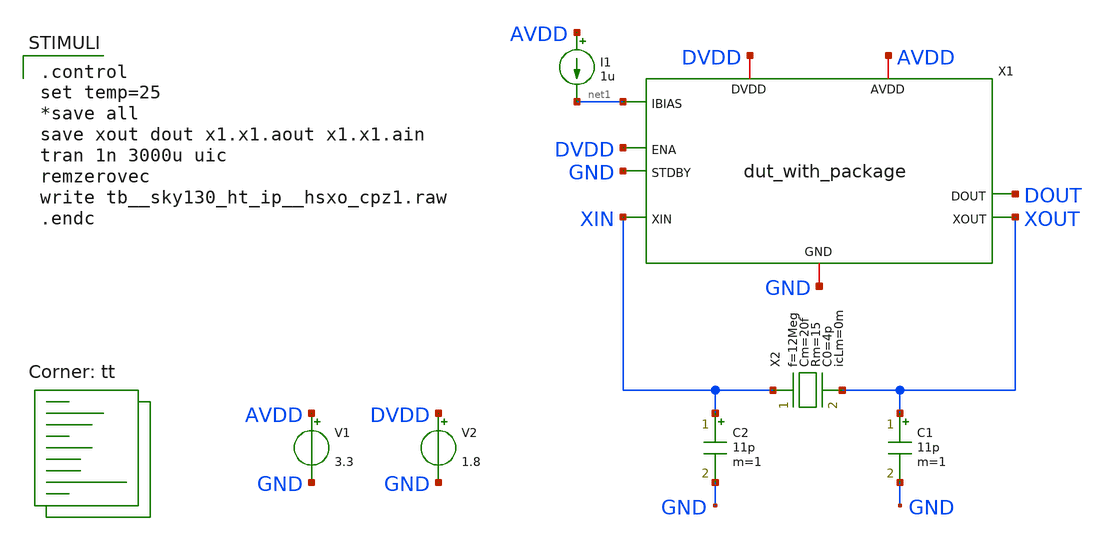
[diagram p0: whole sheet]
** sch_path: xschem/tb__sky130_ht_ip__hsxo_cpz1.sch
**.subckt tb__sky130_ht_ip__hsxo_cpz1
X1 XOUT XIN DVDD GND DOUT AVDD DVDD GND net1 dut_with_package
C1 XOUT GND 11p m=1
C2 XIN GND 11p m=1
I1 AVDD net1 1u
V1 AVDD GND 3.3
V2 DVDD GND 1.8
X2 XIN XOUT crystal_model_p_res f=12Meg Cm=20f Rm=15 C0=4p icLm=0m
**** begin user architecture code
.lib $::SKYWATER_MODELS/sky130.lib.spice tt

.control
set temp=25
*save all
save xout dout x1.x1.aout x1.x1.ain
tran 1n 3000u uic
remzerovec
write tb__sky130_ht_ip__hsxo_cpz1.raw
.endc


**** end user architecture code
**.ends

* expanding   symbol:  dut_with_package.sym # of pins=9
** sym_path: xschem/dut_with_package.sym
** sch_path: xschem/dut_with_package.sch
.subckt dut_with_package XOUT XIN ENA STDBY DOUT AVDD DVDD GND IBIAS
*.iopin DVDD
*.iopin GND
*.iopin AVDD
*.ipin ENA
*.ipin STDBY
*.ipin XIN
*.opin XOUT
*.opin DOUT
*.ipin IBIAS
X1 XOUTPAD XINPAD ENA STDBY DOUT AVDD DVDD AVSS GND IBIAS sky130_ht_ip__hsxo_cpz1
X2 XIN GND XINPAD XOUTPAD XOUT GND AVSS package_model
.ends


* expanding   symbol:  crystal_model_p_res.sym # of pins=2
** sym_path: xschem/crystal_model_p_res.sym
** sch_path: xschem/crystal_model_p_res.sch
.subckt crystal_model_p_res XIN XOUT  f=12Meg Cm=20f Rm=15 C0=4p icLm=0m
*.iopin XIN
*.iopin XOUT
X1 XIN XOUT crystal_model Lm=(1/Cm+1/C0)/(4*pi^2*f^2) Cm=Cm Rm=Rm C0=C0 icLm=icLm
**** begin user architecture code
.param pi=4*atan(1)
**** end user architecture code
.ends


* expanding   symbol:  sky130_ht_ip__hsxo_cpz1.sym # of pins=10
** sym_path: xschem/sky130_ht_ip__hsxo_cpz1.sym
** sch_path: xschem/sky130_ht_ip__hsxo_cpz1.sch
.subckt sky130_ht_ip__hsxo_cpz1 XOUT XIN ENA STDBY DOUT AVDD DVDD AVSS DVSS IBIAS
*.iopin DVDD
*.iopin DVSS
*.iopin AVDD
*.iopin AVSS
*.ipin ENA
*.ipin STDBY
*.ipin XIN
*.opin XOUT
*.opin DOUT
*.ipin IBIAS
x1 XOUT SG_AVDD EG_AVDD XIN EG_IBIAS AOUT SG_AVSS EG_AVSS vittoz_pierce_osc
x2 SG_DVDD AIN DOUT SG_DVSS schmitt_trigger_pullmid
XC1 AOUT AIN sky130_fd_pr__cap_mim_m3_1 W=15 L=15 MF=6 m=6
x3 DOUT SG_AVDD DVDD EG_IBIAS SG_DVDD AVDD IBIAS EG_AVDD ENA SG_DVSS SG_AVSS STDBY EG_AVSS AVSS DVSS
+ XIN power_gating
.ends


* expanding   symbol:  package_model.sym # of pins=7
** sym_path: xschem/package_model.sym
** sch_path: xschem/package_model.sch
.subckt package_model PIN1 GND PAD1 PAD2 PIN2 PIN3 PAD3
*.iopin PAD1
*.iopin PAD2
*.iopin PIN1
*.iopin PIN2
*.iopin GND
*.iopin PAD3
*.iopin PIN3
R1 net9 net1 0.1 m=1
L1 net1 PAD1 2.57n m=1
C1 net2 GND 50f m=1
C12 net2 net4 200f m=1
K1 L1 L2 0.57
R2 net10 net3 0.1 m=1
L2 net3 PAD2 2.57n m=1
C2 net4 GND 50f m=1
R4 net5 net9 0.14 m=1
R5 net6 net10 0.14 m=1
L4 net2 net5 1.2n m=1
K4 L4 L5 0.54
L5 net4 net6 1.2n m=1
L7 net7 net2 1.2n m=1
K7 L7 L8 0.54
L8 net8 net4 1.2n m=1
R7 PIN1 net7 0.14 m=1
R8 PIN2 net8 0.14 m=1
R3 net15 net11 0.1 m=1
L3 net11 PAD3 2.57n m=1
C3 net12 GND 50f m=1
R6 net13 net15 0.14 m=1
L6 net12 net13 1.2n m=1
L9 net14 net12 1.2n m=1
R9 PIN3 net14 0.14 m=1
K2 L2 L3 0.57
K3 L3 L1 0.44
K5 L5 L6 0.54
K6 L6 L4 0.38
C23 net4 net12 200f m=1
C13 net2 net12 200f m=1
K8 L8 L9 0.54
K9 L9 L7 0.38
.ends


* expanding   symbol:  crystal_model.sym # of pins=2
** sym_path: xschem/crystal_model.sym
** sch_path: xschem/crystal_model.sch
.subckt crystal_model XIN XOUT  Lm=8.8m Cm=20f Rm=15 C0=4p icLm=0m
*.iopin XIN
*.iopin XOUT
Cm net1 net2 C=Cm m=1
Lm XIN net1 L=Lm ic=icLm m=1
Rm net2 XOUT R=Rm m=1
C0 XIN XOUT C=C0 m=1
.ends


* expanding   symbol:  vittoz_pierce_osc.sym # of pins=8
** sym_path: xschem/vittoz_pierce_osc.sym
** sch_path: xschem/vittoz_pierce_osc.sch
.subckt vittoz_pierce_osc XOUT SG_AVDD EG_AVDD XIN EG_IBIAS AOUT SG_AVSS EG_AVSS
*.iopin EG_AVDD
*.iopin EG_AVSS
*.iopin SG_AVDD
*.iopin SG_AVSS
*.ipin XIN
*.ipin EG_IBIAS
*.opin XOUT
*.opin AOUT
XM9 net6 PBIAS EG_AVDD EG_AVDD sky130_fd_pr__pfet_g5v0d10v5 L=0.5 W=1024 nf=32 ad='int((nf+1)/2) * W/nf * 0.29'
+ as='int((nf+2)/2) * W/nf * 0.29' pd='2*int((nf+1)/2) * (W/nf + 0.29)' ps='2*int((nf+2)/2) * (W/nf + 0.29)'
+ nrd='0.29 / W' nrs='0.29 / W' sa=0 sb=0 sd=0 mult=1 m=1
XM10 net7 PBIAS EG_AVDD EG_AVDD sky130_fd_pr__pfet_g5v0d10v5 L=0.5 W=128 nf=4 ad='int((nf+1)/2) * W/nf * 0.29'
+ as='int((nf+2)/2) * W/nf * 0.29' pd='2*int((nf+1)/2) * (W/nf + 0.29)' ps='2*int((nf+2)/2) * (W/nf + 0.29)'
+ nrd='0.29 / W' nrs='0.29 / W' sa=0 sb=0 sd=0 mult=1 m=1
XM11 PBIAS PBIAS EG_AVDD EG_AVDD sky130_fd_pr__pfet_g5v0d10v5 L=0.5 W=128 nf=4 ad='int((nf+1)/2) * W/nf * 0.29'
+ as='int((nf+2)/2) * W/nf * 0.29' pd='2*int((nf+1)/2) * (W/nf + 0.29)' ps='2*int((nf+2)/2) * (W/nf + 0.29)'
+ nrd='0.29 / W' nrs='0.29 / W' sa=0 sb=0 sd=0 mult=1 m=1
Vmeas3 net6 XOUT 0
.save i(vmeas3)
Vmeas4 net7 net1 0
.save i(vmeas4)
Vmeas2 PBIAS net3 0
.save i(vmeas2)
XM12 net1 net2 EG_AVSS EG_AVSS sky130_fd_pr__nfet_g5v0d10v5 L=0.5 W=128 nf=4 ad='int((nf+1)/2) * W/nf * 0.29'
+ as='int((nf+2)/2) * W/nf * 0.29' pd='2*int((nf+1)/2) * (W/nf + 0.29)' ps='2*int((nf+2)/2) * (W/nf + 0.29)'
+ nrd='0.29 / W' nrs='0.29 / W' sa=0 sb=0 sd=0 mult=1 m=1
XR1 net2 net1 EG_AVSS sky130_fd_pr__res_xhigh_po_0p35 L=7 mult=1 m=1
XC1 net1 EG_AVSS sky130_fd_pr__cap_mim_m3_1 W=2 L=2 MF=1 m=1
XC2 XIN net2 sky130_fd_pr__cap_mim_m3_1 W=15 L=15 MF=6 m=6
XC7 net2 EG_AVSS sky130_fd_pr__cap_mim_m3_1 W=15 L=15 MF=6 m=6
XM13 XOUT XIN EG_AVSS EG_AVSS sky130_fd_pr__nfet_g5v0d10v5 L=0.5 W=32 nf=8 ad='int((nf+1)/2) * W/nf * 0.29'
+ as='int((nf+2)/2) * W/nf * 0.29' pd='2*int((nf+1)/2) * (W/nf + 0.29)' ps='2*int((nf+2)/2) * (W/nf + 0.29)'
+ nrd='0.29 / W' nrs='0.29 / W' sa=0 sb=0 sd=0 mult=1 m=1
XM14 net3 net2 net5 EG_AVSS sky130_fd_pr__nfet_g5v0d10v5 L=0.5 W=1024 nf=32 ad='int((nf+1)/2) * W/nf * 0.29'
+ as='int((nf+2)/2) * W/nf * 0.29' pd='2*int((nf+1)/2) * (W/nf + 0.29)' ps='2*int((nf+2)/2) * (W/nf + 0.29)'
+ nrd='0.29 / W' nrs='0.29 / W' sa=0 sb=0 sd=0 mult=1 m=1
XM15 net5 net4 EG_AVSS EG_AVSS sky130_fd_pr__nfet_g5v0d10v5 L=0.5 W=128 nf=4 ad='int((nf+1)/2) * W/nf * 0.29'
+ as='int((nf+2)/2) * W/nf * 0.29' pd='2*int((nf+1)/2) * (W/nf + 0.29)' ps='2*int((nf+2)/2) * (W/nf + 0.29)'
+ nrd='0.29 / W' nrs='0.29 / W' sa=0 sb=0 sd=0 mult=1 m=1
XM16 net4 net4 EG_AVSS EG_AVSS sky130_fd_pr__nfet_g5v0d10v5 L=0.5 W=8 nf=1 ad='int((nf+1)/2) * W/nf * 0.29'
+ as='int((nf+2)/2) * W/nf * 0.29' pd='2*int((nf+1)/2) * (W/nf + 0.29)' ps='2*int((nf+2)/2) * (W/nf + 0.29)'
+ nrd='0.29 / W' nrs='0.29 / W' sa=0 sb=0 sd=0 mult=1 m=1
XR3 XIN XOUT EG_AVSS sky130_fd_pr__res_xhigh_po_0p35 L=2.8 mult=1 m=1
XM17 AOUT XIN SG_AVSS SG_AVSS sky130_fd_pr__nfet_g5v0d10v5 L=0.5 W=4 nf=1 ad='int((nf+1)/2) * W/nf * 0.29'
+ as='int((nf+2)/2) * W/nf * 0.29' pd='2*int((nf+1)/2) * (W/nf + 0.29)' ps='2*int((nf+2)/2) * (W/nf + 0.29)'
+ nrd='0.29 / W' nrs='0.29 / W' sa=0 sb=0 sd=0 mult=1 m=1
XM18 net8 PBIAS SG_AVDD SG_AVDD sky130_fd_pr__pfet_g5v0d10v5 L=0.5 W=128 nf=4 ad='int((nf+1)/2) * W/nf * 0.29'
+ as='int((nf+2)/2) * W/nf * 0.29' pd='2*int((nf+1)/2) * (W/nf + 0.29)' ps='2*int((nf+2)/2) * (W/nf + 0.29)'
+ nrd='0.29 / W' nrs='0.29 / W' sa=0 sb=0 sd=0 mult=1 m=1
Vmeas5 net8 AOUT 0
.save i(vmeas5)
XC8 AOUT SG_AVSS sky130_fd_pr__cap_mim_m3_1 W=2 L=2 MF=1 m=1
XC3 EG_AVDD EG_AVSS sky130_fd_pr__cap_mim_m3_1 W=15 L=15 MF=6 m=6
XC4 SG_AVDD SG_AVSS sky130_fd_pr__cap_mim_m3_1 W=15 L=15 MF=6 m=6
Vmeas1 EG_IBIAS net4 0
.save i(vmeas1)
.ends


* expanding   symbol:  schmitt_trigger_pullmid.sym # of pins=4
** sym_path: xschem/schmitt_trigger_pullmid.sym
** sch_path: xschem/schmitt_trigger_pullmid.sch
.subckt schmitt_trigger_pullmid SG_DVDD AIN DOUT SG_DVSS
*.iopin SG_DVDD
*.iopin SG_DVSS
*.ipin AIN
*.opin DOUT
XR3 net2 net1 SG_DVSS sky130_fd_pr__res_xhigh_po_0p35 L=128 mult=1 m=1
XM3 DOUT net2 DHT SG_DVDD sky130_fd_pr__pfet_01v8 L=0.3 W=1 nf=1 ad='int((1 + 1)/2) * 1 / 1 * 0.29' as='int((1 + 2)/2) * 1 / 1 * 0.29'
+ pd='2*int((1 + 1)/2) * (1 / 1 + 0.29)' ps='2*int((1 + 2)/2) * (1 / 1 + 0.29)' nrd='0.29 / 1 ' nrs='0.29 / 1 '
+ sa=0 sb=0 sd=0 mult=1 m=1
XM4 DOUT net2 DLT SG_DVSS sky130_fd_pr__nfet_01v8 L=0.2 W=1 nf=1 ad='int((nf+1)/2) * W/nf * 0.29' as='int((nf+2)/2) * W/nf * 0.29'
+ pd='2*int((nf+1)/2) * (W/nf + 0.29)' ps='2*int((nf+2)/2) * (W/nf + 0.29)' nrd='0.29 / W' nrs='0.29 / W'
+ sa=0 sb=0 sd=0 mult=1 m=1
XM5 DHT net2 SG_DVDD SG_DVDD sky130_fd_pr__pfet_01v8 L=0.3 W=1 nf=1 ad='int((1 + 1)/2) * 1 / 1 * 0.29'
+ as='int((1 + 2)/2) * 1 / 1 * 0.29' pd='2*int((1 + 1)/2) * (1 / 1 + 0.29)' ps='2*int((1 + 2)/2) * (1 / 1 + 0.29)'
+ nrd='0.29 / 1 ' nrs='0.29 / 1 ' sa=0 sb=0 sd=0 mult=1 m=1
XM6 DLT net2 SG_DVSS SG_DVSS sky130_fd_pr__nfet_01v8 L=0.2 W=1 nf=1 ad='int((nf+1)/2) * W/nf * 0.29'
+ as='int((nf+2)/2) * W/nf * 0.29' pd='2*int((nf+1)/2) * (W/nf + 0.29)' ps='2*int((nf+2)/2) * (W/nf + 0.29)'
+ nrd='0.29 / W' nrs='0.29 / W' sa=0 sb=0 sd=0 mult=1 m=1
XM7 SG_DVSS DOUT DHT SG_DVDD sky130_fd_pr__pfet_01v8 L=0.3 W=1 nf=1 ad='int((1 + 1)/2) * 1 / 1 * 0.29'
+ as='int((1 + 2)/2) * 1 / 1 * 0.29' pd='2*int((1 + 1)/2) * (1 / 1 + 0.29)' ps='2*int((1 + 2)/2) * (1 / 1 + 0.29)'
+ nrd='0.29 / 1 ' nrs='0.29 / 1 ' sa=0 sb=0 sd=0 mult=1 m=1
XM8 SG_DVDD DOUT DLT SG_DVSS sky130_fd_pr__nfet_01v8 L=0.2 W=1 nf=1 ad='int((nf+1)/2) * W/nf * 0.29'
+ as='int((nf+2)/2) * W/nf * 0.29' pd='2*int((nf+1)/2) * (W/nf + 0.29)' ps='2*int((nf+2)/2) * (W/nf + 0.29)'
+ nrd='0.29 / W' nrs='0.29 / W' sa=0 sb=0 sd=0 mult=1 m=1
XC4 SG_DVDD SG_DVSS sky130_fd_pr__cap_mim_m3_1 W=15 L=15 MF=6 m=6
XR1 net1 SG_DVDD SG_DVSS sky130_fd_pr__res_xhigh_po_0p35 L=16 mult=1 m=1
XR2 SG_DVSS net1 SG_DVSS sky130_fd_pr__res_xhigh_po_0p35 L=16 mult=1 m=1
Vmeas6 AIN net2 0
.save i(vmeas6)
.ends


* expanding   symbol:  /foss/designs/hsxo-cpz1/xschem/power_gating.sym # of pins=16
** sym_path: xschem/power_gating.sym
** sch_path: xschem/power_gating.sch
.subckt power_gating DOUT SG_AVDD DVDD EG_IBIAS SG_DVDD AVDD IBIAS EG_AVDD ENA SG_DVSS SG_AVSS STDBY
+ EG_AVSS AVSS DVSS XIN
*.iopin DVDD
*.iopin DVSS
*.iopin AVDD
*.iopin AVSS
*.ipin ENA
*.ipin STDBY
*.opin DOUT
*.ipin IBIAS
*.iopin EG_AVDD
*.iopin EG_AVSS
*.iopin SG_AVDD
*.iopin SG_AVSS
*.iopin SG_DVDD
*.iopin SG_DVSS
*.opin EG_IBIAS
*.ipin XIN
x3 AVDD ENA_B DVDD ENA ENA_H AVSS DVSS ENA_BH level_shifter
x4 AVDD STDBY_B DVDD STDBY STDBY_H AVSS DVSS STDBY_BH level_shifter
XM18 SG_DVSS STDBY_B DVSS DVSS sky130_fd_pr__nfet_01v8 L=0.15 W=8 nf=4 ad='int((nf+1)/2) * W/nf * 0.29'
+ as='int((nf+2)/2) * W/nf * 0.29' pd='2*int((nf+1)/2) * (W/nf + 0.29)' ps='2*int((nf+2)/2) * (W/nf + 0.29)'
+ nrd='0.29 / W' nrs='0.29 / W' sa=0 sb=0 sd=0 mult=1 m=1
XM21 EG_AVSS ENA_H AVSS AVSS sky130_fd_pr__nfet_g5v0d10v5 L=0.5 W=8 nf=4 ad='int((nf+1)/2) * W/nf * 0.29'
+ as='int((nf+2)/2) * W/nf * 0.29' pd='2*int((nf+1)/2) * (W/nf + 0.29)' ps='2*int((nf+2)/2) * (W/nf + 0.29)'
+ nrd='0.29 / W' nrs='0.29 / W' sa=0 sb=0 sd=0 mult=1 m=1
XM25 EG_AVDD ENA_BH AVDD AVDD sky130_fd_pr__pfet_g5v0d10v5 L=0.5 W=8 nf=4 ad='int((nf+1)/2) * W/nf * 0.29'
+ as='int((nf+2)/2) * W/nf * 0.29' pd='2*int((nf+1)/2) * (W/nf + 0.29)' ps='2*int((nf+2)/2) * (W/nf + 0.29)'
+ nrd='0.29 / W' nrs='0.29 / W' sa=0 sb=0 sd=0 mult=1 m=1
XM27 SG_DVDD STDBY DVDD DVDD sky130_fd_pr__pfet_01v8 L=0.15 W=8 nf=4 ad='int((4 + 1)/2) * 8 / 4 * 0.29'
+ as='int((4 + 2)/2) * 8 / 4 * 0.29' pd='2*int((4 + 1)/2) * (8 / 4 + 0.29)' ps='2*int((4 + 2)/2) * (8 / 4 + 0.29)'
+ nrd='0.29 / 8 ' nrs='0.29 / 8 ' sa=0 sb=0 sd=0 mult=1 m=1
XM1 SG_AVDD STDBY_H AVDD AVDD sky130_fd_pr__pfet_g5v0d10v5 L=0.5 W=8 nf=4 ad='int((nf+1)/2) * W/nf * 0.29'
+ as='int((nf+2)/2) * W/nf * 0.29' pd='2*int((nf+1)/2) * (W/nf + 0.29)' ps='2*int((nf+2)/2) * (W/nf + 0.29)'
+ nrd='0.29 / W' nrs='0.29 / W' sa=0 sb=0 sd=0 mult=1 m=1
XM2 EG_IBIAS ENA_BH IBIAS AVDD sky130_fd_pr__pfet_g5v0d10v5 L=0.5 W=8 nf=4 ad='int((nf+1)/2) * W/nf * 0.29'
+ as='int((nf+2)/2) * W/nf * 0.29' pd='2*int((nf+1)/2) * (W/nf + 0.29)' ps='2*int((nf+2)/2) * (W/nf + 0.29)'
+ nrd='0.29 / W' nrs='0.29 / W' sa=0 sb=0 sd=0 mult=1 m=1
XM3 SG_AVSS STDBY_BH AVSS AVSS sky130_fd_pr__nfet_g5v0d10v5 L=0.5 W=8 nf=4 ad='int((nf+1)/2) * W/nf * 0.29'
+ as='int((nf+2)/2) * W/nf * 0.29' pd='2*int((nf+1)/2) * (W/nf + 0.29)' ps='2*int((nf+2)/2) * (W/nf + 0.29)'
+ nrd='0.29 / W' nrs='0.29 / W' sa=0 sb=0 sd=0 mult=1 m=1
XM4 DOUT STDBY DVSS DVSS sky130_fd_pr__nfet_01v8 L=0.15 W=8 nf=4 ad='int((nf+1)/2) * W/nf * 0.29' as='int((nf+2)/2) * W/nf * 0.29'
+ pd='2*int((nf+1)/2) * (W/nf + 0.29)' ps='2*int((nf+2)/2) * (W/nf + 0.29)' nrd='0.29 / W' nrs='0.29 / W'
+ sa=0 sb=0 sd=0 mult=1 m=1
XC3 AVDD AVSS sky130_fd_pr__cap_mim_m3_1 W=15 L=15 MF=6 m=6
XC4 DVDD DVSS sky130_fd_pr__cap_mim_m3_1 W=15 L=15 MF=6 m=6
XD1 XIN AVDD sky130_fd_pr__diode_pd2nw_05v5 area=2e11 pj=1.8e6
XD2 AVSS XIN sky130_fd_pr__diode_pw2nd_05v5 area=2e11 pj=1.8e6
.ends


* expanding   symbol:  level_shifter.sym # of pins=8
** sym_path: xschem/level_shifter.sym
** sch_path: xschem/level_shifter.sch
.subckt level_shifter AVDD LO_B DVDD LO HI AVSS DVSS HI_B
*.iopin DVDD
*.iopin DVSS
*.iopin AVDD
*.iopin AVSS
*.ipin LO
*.opin LO_B
*.opin HI
*.opin HI_B
XM18 LO_B LO DVSS DVSS sky130_fd_pr__nfet_01v8 L=0.15 W=1 nf=1 ad='int((nf+1)/2) * W/nf * 0.29' as='int((nf+2)/2) * W/nf * 0.29'
+ pd='2*int((nf+1)/2) * (W/nf + 0.29)' ps='2*int((nf+2)/2) * (W/nf + 0.29)' nrd='0.29 / W' nrs='0.29 / W'
+ sa=0 sb=0 sd=0 mult=1 m=1
XM21 HI_B LO AVSS AVSS sky130_fd_pr__nfet_g5v0d10v5 L=0.5 W=1 nf=1 ad='int((nf+1)/2) * W/nf * 0.29' as='int((nf+2)/2) * W/nf * 0.29'
+ pd='2*int((nf+1)/2) * (W/nf + 0.29)' ps='2*int((nf+2)/2) * (W/nf + 0.29)' nrd='0.29 / W' nrs='0.29 / W'
+ sa=0 sb=0 sd=0 mult=1 m=1
XM25 HI_B HI AVDD AVDD sky130_fd_pr__pfet_g5v0d10v5 L=0.5 W=1 nf=1 ad='int((nf+1)/2) * W/nf * 0.29' as='int((nf+2)/2) * W/nf * 0.29'
+ pd='2*int((nf+1)/2) * (W/nf + 0.29)' ps='2*int((nf+2)/2) * (W/nf + 0.29)' nrd='0.29 / W' nrs='0.29 / W'
+ sa=0 sb=0 sd=0 mult=1 m=1
XM27 LO_B LO DVDD DVDD sky130_fd_pr__pfet_01v8 L=0.15 W=1 nf=1 ad='int((1 + 1)/2) * 1 / 1 * 0.29' as='int((1 + 2)/2) * 1 / 1 * 0.29'
+ pd='2*int((1 + 1)/2) * (1 / 1 + 0.29)' ps='2*int((1 + 2)/2) * (1 / 1 + 0.29)' nrd='0.29 / 1 ' nrs='0.29 / 1 '
+ sa=0 sb=0 sd=0 mult=1 m=1
XM1 HI HI_B AVDD AVDD sky130_fd_pr__pfet_g5v0d10v5 L=0.5 W=1 nf=1 ad='int((nf+1)/2) * W/nf * 0.29' as='int((nf+2)/2) * W/nf * 0.29'
+ pd='2*int((nf+1)/2) * (W/nf + 0.29)' ps='2*int((nf+2)/2) * (W/nf + 0.29)' nrd='0.29 / W' nrs='0.29 / W'
+ sa=0 sb=0 sd=0 mult=1 m=1
XM2 HI LO_B AVSS AVSS sky130_fd_pr__nfet_g5v0d10v5 L=0.5 W=1 nf=1 ad='int((nf+1)/2) * W/nf * 0.29' as='int((nf+2)/2) * W/nf * 0.29'
+ pd='2*int((nf+1)/2) * (W/nf + 0.29)' ps='2*int((nf+2)/2) * (W/nf + 0.29)' nrd='0.29 / W' nrs='0.29 / W'
+ sa=0 sb=0 sd=0 mult=1 m=1
.ends

.end
